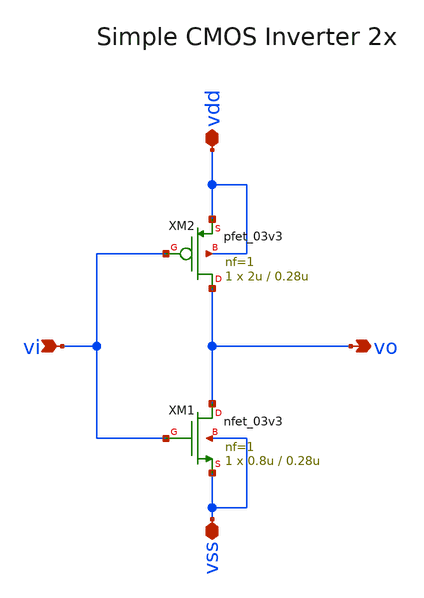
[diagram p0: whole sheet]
** sch_path: designs/comparator/inv2x.sch
**.subckt inv2x vdd vss vi vo
*.iopin vdd
*.iopin vss
*.ipin vi
*.opin vo
XM1 vo vi vss vss nfet_03v3 L=0.28u W=0.8u nf=1 ad='int((nf+1)/2) * W/nf * 0.18u' as='int((nf+2)/2) * W/nf * 0.18u'
+ pd='2*int((nf+1)/2) * (W/nf + 0.18u)' ps='2*int((nf+2)/2) * (W/nf + 0.18u)' nrd='0.18u / W' nrs='0.18u / W'
+ sa=0 sb=0 sd=0 m=1
XM2 vo vi vdd vdd pfet_03v3 L=0.28u W=2u nf=1 ad='int((nf+1)/2) * W/nf * 0.18u' as='int((nf+2)/2) * W/nf * 0.18u'
+ pd='2*int((nf+1)/2) * (W/nf + 0.18u)' ps='2*int((nf+2)/2) * (W/nf + 0.18u)' nrd='0.18u / W' nrs='0.18u / W'
+ sa=0 sb=0 sd=0 m=1
**.ends
.end
